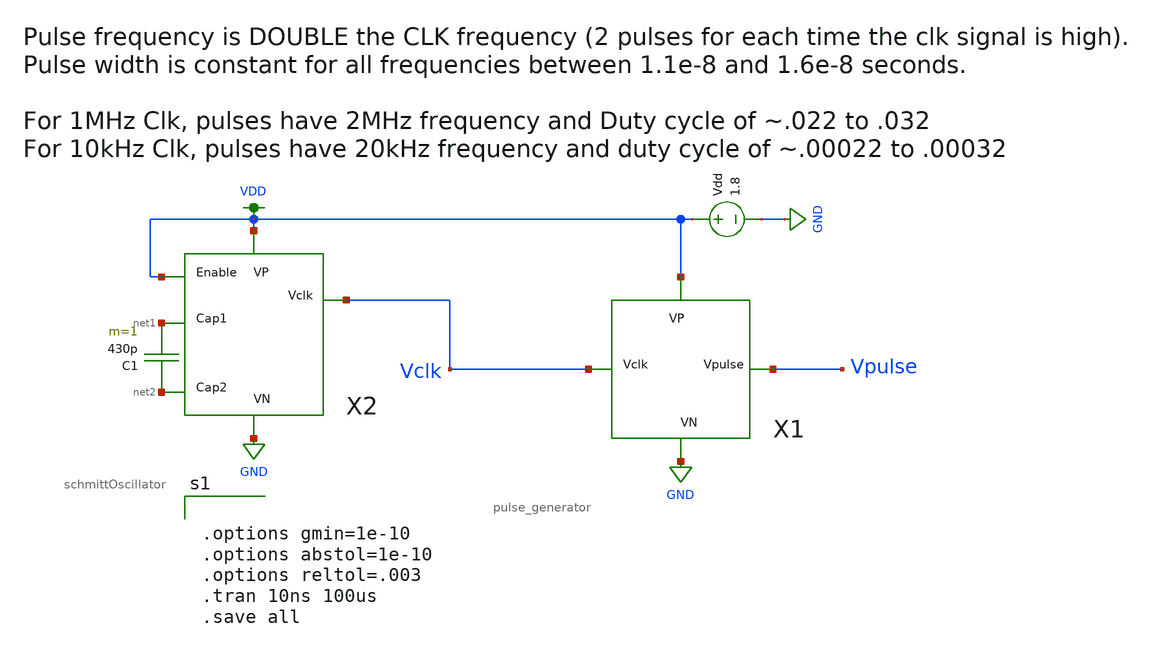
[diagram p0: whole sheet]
** sch_path: schematics/pulse_generator_testbench.sch
**.subckt pulse_generator_testbench
Vdd VDD GND 1.8
X2 VDD net1 net2 VDD GND Vclk schmittOscillator
C1 net2 net1 430p m=1
X1 Vpulse VDD GND Vclk pulse_generator
**** begin user architecture code


.options gmin=1e-10
.options abstol=1e-10
.options reltol=.003
.tran 10ns 100us
.save all


.option wnflag=1
.lib ~/skywater/skywater-pdk/libraries/sky130_fd_pr_ngspice/latest/models/sky130.lib.spice tt

**** end user architecture code
**.ends
.GLOBAL GND
.GLOBAL VDD
.end
